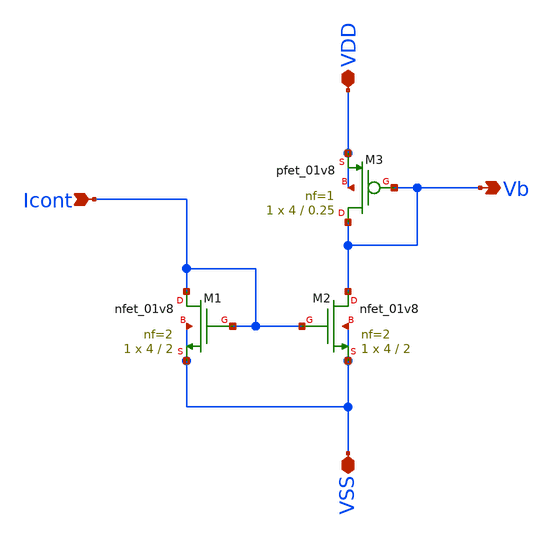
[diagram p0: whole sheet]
** sch_path: xschem/vco_bias.sch
**.subckt vco_bias VDD VSS Icont Vb
*.iopin VDD
*.iopin VSS
*.ipin Icont
*.opin Vb
XM1 Icont Icont VSS VSS sky130_fd_pr__nfet_01v8 L=2 W=4 nf=2 ad='int((nf+1)/2) * W/nf * 0.29' as='int((nf+2)/2) * W/nf * 0.29'
+ pd='2*int((nf+1)/2) * (W/nf + 0.29)' ps='2*int((nf+2)/2) * (W/nf + 0.29)' nrd='0.29 / W' nrs='0.29 / W'
+ sa=0 sb=0 sd=0 mult=1 m=1
XM2 Vb Icont VSS VSS sky130_fd_pr__nfet_01v8 L=2 W=4 nf=2 ad='int((nf+1)/2) * W/nf * 0.29' as='int((nf+2)/2) * W/nf * 0.29'
+ pd='2*int((nf+1)/2) * (W/nf + 0.29)' ps='2*int((nf+2)/2) * (W/nf + 0.29)' nrd='0.29 / W' nrs='0.29 / W'
+ sa=0 sb=0 sd=0 mult=1 m=1
XM3 Vb Vb VDD VDD sky130_fd_pr__pfet_01v8 L=0.25 W=4 nf=1 ad='int((nf+1)/2) * W/nf * 0.29' as='int((nf+2)/2) * W/nf * 0.29'
+ pd='2*int((nf+1)/2) * (W/nf + 0.29)' ps='2*int((nf+2)/2) * (W/nf + 0.29)' nrd='0.29 / W' nrs='0.29 / W'
+ sa=0 sb=0 sd=0 mult=1 m=1
**.ends
.end
